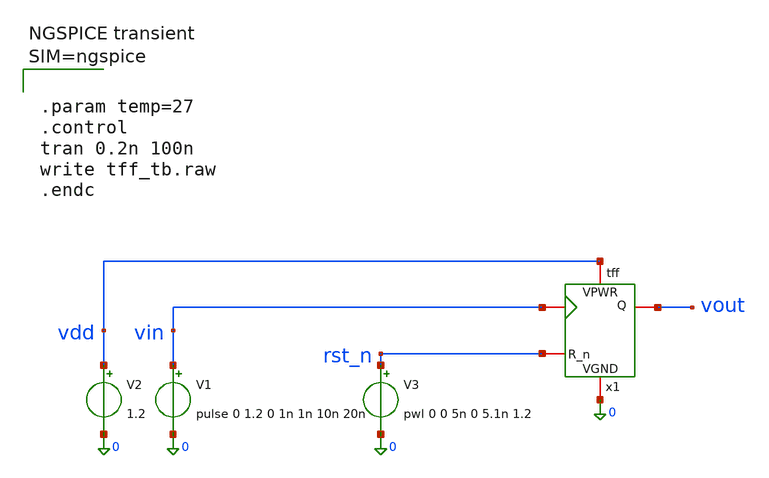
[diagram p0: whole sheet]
** sch_path: digital/div16/xschem/tff_tb.sch
**.subckt tff_tb
x1 0 vdd vin vout rst_n tff
V1 vin 0 pulse 0 1.2 0 1n 1n 10n 20n
V2 vdd 0 1.2
V3 rst_n 0 pwl 0 0 5n 0 5.1n 1.2
**** begin user architecture code



.include /foss/pdks/ihp-sg13cmos5l/libs.ref/sg13cmos5l_stdcell/spice/sg13cmos5l_stdcell.spice






.lib cornerMOSlv.lib mos_tt
.lib cornerMOShv.lib mos_tt
.lib cornerRES.lib res_typ
.lib cornerDIO.lib dio_tt






.param temp=27
.control
tran 0.2n 100n
write tff_tb.raw
.endc



**** end user architecture code
**.ends

* expanding   symbol:  digital/tff/xschem/tff.sym # of pins=5
** sym_path: digital/div16/xschem/tff.sym

.include /foss/designs/digital/tff/xschem/tff.spice

.end
